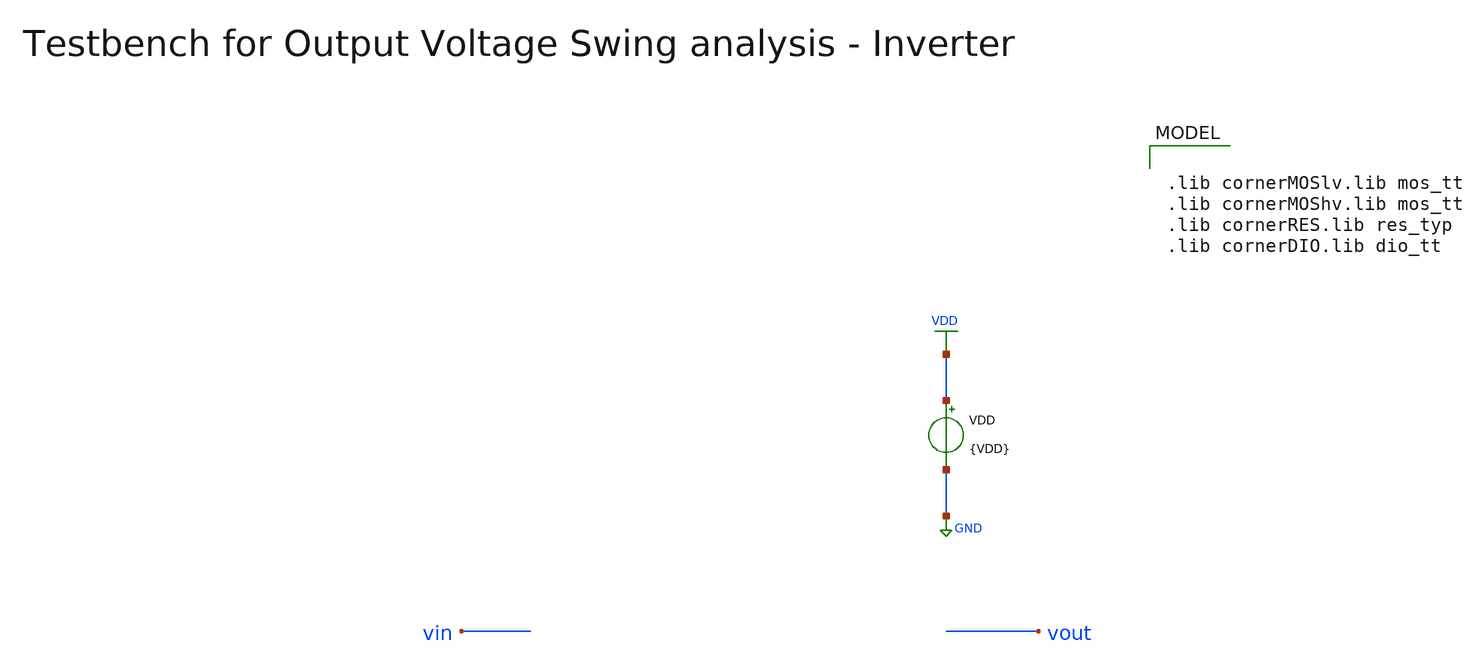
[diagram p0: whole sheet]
** sch_path: inverter/testbenches/xschem/inverter_tb_dc_vout.sch
**.subckt inverter_tb_dc_vout
VDD VDD GND {VDD}
**** begin user architecture code


*.include ../../../netlist/pex/inverter_magic_pex_3.spice
.param VDD=1.5
.csparam VDD=VDD
.param Vcm=VDD/2
.csparam Vcm=Vcm
.param temp=27
.param Cload=10p
.param Rload=1k
.options savecurrents klu method=gear reltol=1e-3 abstol=1e-15 gmin=1e-15
.control

save all

* Operating Point Analysis
op
remzerovec
write @schname\.raw
set appendwrite

* DC Sweep
dc Vgsp 0 $&VDD 1m
remzerovec
write @schname\.raw
set appendwrite

* Plotting
plot vin vout

* Measurement
meas dc Vgsp_at_Vcm when vout=Vcm
print Vgsp_at_Vcm

* Write Data
unset appendwrite
set wr_vecnames
set wr_singlescale
wrdata ../plot_simulations/data/@schname\.txt v(vin) v(vout)

*quit
.endc



.lib cornerMOSlv.lib mos_tt
.lib cornerMOShv.lib mos_tt
.lib cornerRES.lib res_typ
.lib cornerDIO.lib dio_tt

**** end user architecture code
**.ends
.GLOBAL GND
.GLOBAL VDD
.end
